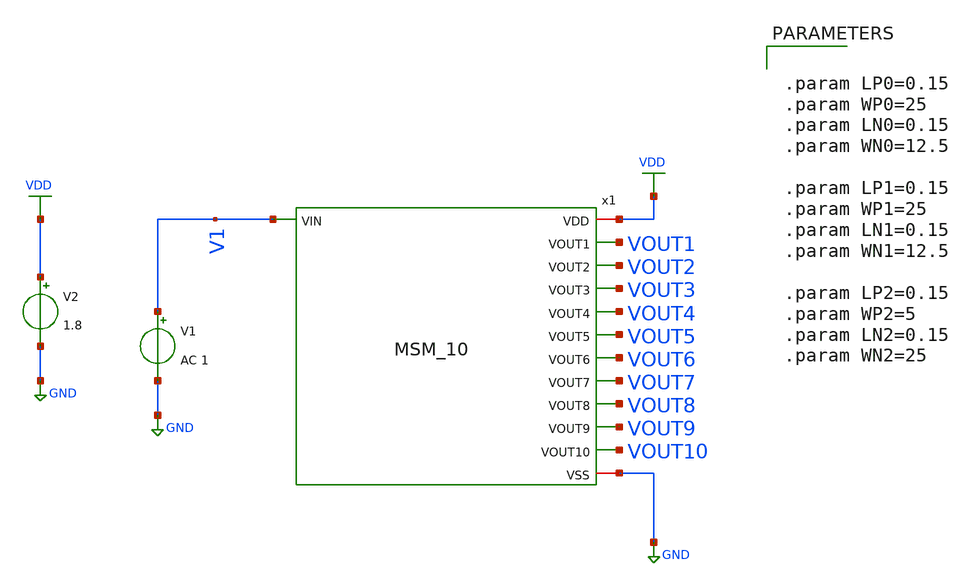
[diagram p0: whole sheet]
** sch_path: LIQAF circuit/10-Stage/DC Sweep.sch
**.subckt DC Sweep
V1 V1 GND AC 1
V2 VDD GND 1.8
x1 VDD VOUT1 VOUT2 V1 VOUT3 VOUT4 VOUT5 VOUT6 VOUT7 VOUT8 VOUT9 VOUT10 GND MSM_10
**** begin user architecture code
 ** manual skywater pdks install (with patches applied)
* .lib $::SKYWATER_MODELS/models/sky130.lib.spice tt

** opencircuitdesign pdks install
.lib $::SKYWATER_MODELS/sky130.lib.spice tt

.param mc_mm_switch=0
.param mc_pr_switch=0


.dc V1 0 1.8 0.01
.control
run
plot v(V1) v(VOUT1) v(VOUT2) v(VOUT3) v(VOUT4) v(VOUT5) v(VOUT6) v(VOUT7) v(VOUT8) v(VOUT9)
+ v(VOUT10)
.endc
.save all



.param LP0=0.15
.param WP0=25
.param LN0=0.15
.param WN0=12.5

.param LP1=0.15
.param WP1=25
.param LN1=0.15
.param WN1=12.5

.param LP2=0.15
.param WP2=5
.param LN2=0.15
.param WN2=25


**** end user architecture code
**.ends

* expanding   symbol:  /home/sudhar/Documents/VLSI/Analog-MSM-Array/LIQAF
*+ circuit/10-Stage/MSM_10.sym # of pins=13
** sym_path: LIQAF circuit/10-Stage/MSM_10.sym
** sch_path: LIQAF circuit/10-Stage/MSM_10.sch
.subckt MSM_10 VDD VOUT1 VOUT2 VIN VOUT3 VOUT4 VOUT5 VOUT6 VOUT7 VOUT8 VOUT9 VOUT10 VSS
*.ipin VIN
*.iopin VDD
*.iopin VSS
*.opin VOUT1
*.opin VOUT2
*.opin VOUT3
*.opin VOUT4
*.opin VOUT5
*.opin VOUT6
*.opin VOUT7
*.opin VOUT8
*.opin VOUT9
*.opin VOUT10
XM1 VOUT1 VIN VOUT2 VSS sky130_fd_pr__nfet_01v8 L=LN1 W=WN1 nf=1 ad='int((nf+1)/2) * W/nf * 0.29' as='int((nf+2)/2) * W/nf * 0.29'
+ pd='2*int((nf+1)/2) * (W/nf + 0.29)' ps='2*int((nf+2)/2) * (W/nf + 0.29)' nrd='0.29 / W' nrs='0.29 / W'
+ sa=0 sb=0 sd=0 mult=1 m=1
XM2 VOUT10 VIN VSS VSS sky130_fd_pr__nfet_01v8 L=LN0 W=WN0 nf=1 ad='int((nf+1)/2) * W/nf * 0.29' as='int((nf+2)/2) * W/nf * 0.29'
+ pd='2*int((nf+1)/2) * (W/nf + 0.29)' ps='2*int((nf+2)/2) * (W/nf + 0.29)' nrd='0.29 / W' nrs='0.29 / W'
+ sa=0 sb=0 sd=0 mult=1 m=1
XM3 VOUT2 VIN VOUT1 VDD sky130_fd_pr__pfet_01v8 L=LP1 W=WP1 nf=1 ad='int((nf+1)/2) * W/nf * 0.29' as='int((nf+2)/2) * W/nf * 0.29'
+ pd='2*int((nf+1)/2) * (W/nf + 0.29)' ps='2*int((nf+2)/2) * (W/nf + 0.29)' nrd='0.29 / W' nrs='0.29 / W'
+ sa=0 sb=0 sd=0 mult=1 m=1
XM4 VOUT1 VIN VDD VDD sky130_fd_pr__pfet_01v8 L=LP0 W=WP0 nf=1 ad='int((nf+1)/2) * W/nf * 0.29' as='int((nf+2)/2) * W/nf * 0.29'
+ pd='2*int((nf+1)/2) * (W/nf + 0.29)' ps='2*int((nf+2)/2) * (W/nf + 0.29)' nrd='0.29 / W' nrs='0.29 / W'
+ sa=0 sb=0 sd=0 mult=1 m=1
XM5 VOUT1 VDD net1 VSS sky130_fd_pr__nfet_01v8 L=LN2 W=WN2 nf=1 ad='int((nf+1)/2) * W/nf * 0.29' as='int((nf+2)/2) * W/nf * 0.29'
+ pd='2*int((nf+1)/2) * (W/nf + 0.29)' ps='2*int((nf+2)/2) * (W/nf + 0.29)' nrd='0.29 / W' nrs='0.29 / W'
+ sa=0 sb=0 sd=0 mult=1 m=1
XM6 VIN VOUT2 net1 VDD sky130_fd_pr__pfet_01v8 L=LP2 W=WP2 nf=1 ad='int((nf+1)/2) * W/nf * 0.29' as='int((nf+2)/2) * W/nf * 0.29'
+ pd='2*int((nf+1)/2) * (W/nf + 0.29)' ps='2*int((nf+2)/2) * (W/nf + 0.29)' nrd='0.29 / W' nrs='0.29 / W'
+ sa=0 sb=0 sd=0 mult=1 m=1
XM7 VOUT2 VOUT1 net2 VSS sky130_fd_pr__nfet_01v8 L=LN2 W=WN2 nf=1 ad='int((nf+1)/2) * W/nf * 0.29' as='int((nf+2)/2) * W/nf * 0.29'
+ pd='2*int((nf+1)/2) * (W/nf + 0.29)' ps='2*int((nf+2)/2) * (W/nf + 0.29)' nrd='0.29 / W' nrs='0.29 / W'
+ sa=0 sb=0 sd=0 mult=1 m=1
XM8 VIN VOUT3 net2 VDD sky130_fd_pr__pfet_01v8 L=LP2 W=WP2 nf=1 ad='int((nf+1)/2) * W/nf * 0.29' as='int((nf+2)/2) * W/nf * 0.29'
+ pd='2*int((nf+1)/2) * (W/nf + 0.29)' ps='2*int((nf+2)/2) * (W/nf + 0.29)' nrd='0.29 / W' nrs='0.29 / W'
+ sa=0 sb=0 sd=0 mult=1 m=1
XM9 VOUT2 VIN VOUT3 VSS sky130_fd_pr__nfet_01v8 L=LN1 W=WN1 nf=1 ad='int((nf+1)/2) * W/nf * 0.29' as='int((nf+2)/2) * W/nf * 0.29'
+ pd='2*int((nf+1)/2) * (W/nf + 0.29)' ps='2*int((nf+2)/2) * (W/nf + 0.29)' nrd='0.29 / W' nrs='0.29 / W'
+ sa=0 sb=0 sd=0 mult=1 m=1
XM10 VOUT3 VIN VOUT2 VDD sky130_fd_pr__pfet_01v8 L=LP1 W=WP1 nf=1 ad='int((nf+1)/2) * W/nf * 0.29' as='int((nf+2)/2) * W/nf * 0.29'
+ pd='2*int((nf+1)/2) * (W/nf + 0.29)' ps='2*int((nf+2)/2) * (W/nf + 0.29)' nrd='0.29 / W' nrs='0.29 / W'
+ sa=0 sb=0 sd=0 mult=1 m=1
XM11 VOUT3 VIN VOUT4 VSS sky130_fd_pr__nfet_01v8 L=LN1 W=WN1 nf=1 ad='int((nf+1)/2) * W/nf * 0.29' as='int((nf+2)/2) * W/nf * 0.29'
+ pd='2*int((nf+1)/2) * (W/nf + 0.29)' ps='2*int((nf+2)/2) * (W/nf + 0.29)' nrd='0.29 / W' nrs='0.29 / W'
+ sa=0 sb=0 sd=0 mult=1 m=1
XM12 VOUT4 VIN VOUT3 VDD sky130_fd_pr__pfet_01v8 L=LP1 W=WP1 nf=1 ad='int((nf+1)/2) * W/nf * 0.29' as='int((nf+2)/2) * W/nf * 0.29'
+ pd='2*int((nf+1)/2) * (W/nf + 0.29)' ps='2*int((nf+2)/2) * (W/nf + 0.29)' nrd='0.29 / W' nrs='0.29 / W'
+ sa=0 sb=0 sd=0 mult=1 m=1
XM13 VOUT4 VIN VOUT5 VSS sky130_fd_pr__nfet_01v8 L=LN1 W=WN1 nf=1 ad='int((nf+1)/2) * W/nf * 0.29' as='int((nf+2)/2) * W/nf * 0.29'
+ pd='2*int((nf+1)/2) * (W/nf + 0.29)' ps='2*int((nf+2)/2) * (W/nf + 0.29)' nrd='0.29 / W' nrs='0.29 / W'
+ sa=0 sb=0 sd=0 mult=1 m=1
XM14 VOUT5 VIN VOUT4 VDD sky130_fd_pr__pfet_01v8 L=LP1 W=WP1 nf=1 ad='int((nf+1)/2) * W/nf * 0.29' as='int((nf+2)/2) * W/nf * 0.29'
+ pd='2*int((nf+1)/2) * (W/nf + 0.29)' ps='2*int((nf+2)/2) * (W/nf + 0.29)' nrd='0.29 / W' nrs='0.29 / W'
+ sa=0 sb=0 sd=0 mult=1 m=1
XM15 VOUT5 VIN VOUT6 VSS sky130_fd_pr__nfet_01v8 L=LN1 W=WN1 nf=1 ad='int((nf+1)/2) * W/nf * 0.29' as='int((nf+2)/2) * W/nf * 0.29'
+ pd='2*int((nf+1)/2) * (W/nf + 0.29)' ps='2*int((nf+2)/2) * (W/nf + 0.29)' nrd='0.29 / W' nrs='0.29 / W'
+ sa=0 sb=0 sd=0 mult=1 m=1
XM16 VOUT6 VIN VOUT5 VDD sky130_fd_pr__pfet_01v8 L=LP1 W=WP1 nf=1 ad='int((nf+1)/2) * W/nf * 0.29' as='int((nf+2)/2) * W/nf * 0.29'
+ pd='2*int((nf+1)/2) * (W/nf + 0.29)' ps='2*int((nf+2)/2) * (W/nf + 0.29)' nrd='0.29 / W' nrs='0.29 / W'
+ sa=0 sb=0 sd=0 mult=1 m=1
XM17 VOUT6 VIN VOUT7 VSS sky130_fd_pr__nfet_01v8 L=LN1 W=WN1 nf=1 ad='int((nf+1)/2) * W/nf * 0.29' as='int((nf+2)/2) * W/nf * 0.29'
+ pd='2*int((nf+1)/2) * (W/nf + 0.29)' ps='2*int((nf+2)/2) * (W/nf + 0.29)' nrd='0.29 / W' nrs='0.29 / W'
+ sa=0 sb=0 sd=0 mult=1 m=1
XM18 VOUT7 VIN VOUT6 VDD sky130_fd_pr__pfet_01v8 L=LP1 W=WP1 nf=1 ad='int((nf+1)/2) * W/nf * 0.29' as='int((nf+2)/2) * W/nf * 0.29'
+ pd='2*int((nf+1)/2) * (W/nf + 0.29)' ps='2*int((nf+2)/2) * (W/nf + 0.29)' nrd='0.29 / W' nrs='0.29 / W'
+ sa=0 sb=0 sd=0 mult=1 m=1
XM19 VOUT7 VIN VOUT8 VSS sky130_fd_pr__nfet_01v8 L=LN1 W=WN1 nf=1 ad='int((nf+1)/2) * W/nf * 0.29' as='int((nf+2)/2) * W/nf * 0.29'
+ pd='2*int((nf+1)/2) * (W/nf + 0.29)' ps='2*int((nf+2)/2) * (W/nf + 0.29)' nrd='0.29 / W' nrs='0.29 / W'
+ sa=0 sb=0 sd=0 mult=1 m=1
XM20 VOUT8 VIN VOUT7 VDD sky130_fd_pr__pfet_01v8 L=LP1 W=WP1 nf=1 ad='int((nf+1)/2) * W/nf * 0.29' as='int((nf+2)/2) * W/nf * 0.29'
+ pd='2*int((nf+1)/2) * (W/nf + 0.29)' ps='2*int((nf+2)/2) * (W/nf + 0.29)' nrd='0.29 / W' nrs='0.29 / W'
+ sa=0 sb=0 sd=0 mult=1 m=1
XM21 VOUT8 VIN VOUT9 VSS sky130_fd_pr__nfet_01v8 L=LN1 W=WN1 nf=1 ad='int((nf+1)/2) * W/nf * 0.29' as='int((nf+2)/2) * W/nf * 0.29'
+ pd='2*int((nf+1)/2) * (W/nf + 0.29)' ps='2*int((nf+2)/2) * (W/nf + 0.29)' nrd='0.29 / W' nrs='0.29 / W'
+ sa=0 sb=0 sd=0 mult=1 m=1
XM22 VOUT9 VIN VOUT8 VDD sky130_fd_pr__pfet_01v8 L=LP1 W=WP1 nf=1 ad='int((nf+1)/2) * W/nf * 0.29' as='int((nf+2)/2) * W/nf * 0.29'
+ pd='2*int((nf+1)/2) * (W/nf + 0.29)' ps='2*int((nf+2)/2) * (W/nf + 0.29)' nrd='0.29 / W' nrs='0.29 / W'
+ sa=0 sb=0 sd=0 mult=1 m=1
XM23 VOUT9 VIN VOUT10 VSS sky130_fd_pr__nfet_01v8 L=LN1 W=WN1 nf=1 ad='int((nf+1)/2) * W/nf * 0.29' as='int((nf+2)/2) * W/nf * 0.29'
+ pd='2*int((nf+1)/2) * (W/nf + 0.29)' ps='2*int((nf+2)/2) * (W/nf + 0.29)' nrd='0.29 / W' nrs='0.29 / W'
+ sa=0 sb=0 sd=0 mult=1 m=1
XM24 VOUT10 VIN VOUT9 VDD sky130_fd_pr__pfet_01v8 L=LP1 W=WP1 nf=1 ad='int((nf+1)/2) * W/nf * 0.29' as='int((nf+2)/2) * W/nf * 0.29'
+ pd='2*int((nf+1)/2) * (W/nf + 0.29)' ps='2*int((nf+2)/2) * (W/nf + 0.29)' nrd='0.29 / W' nrs='0.29 / W'
+ sa=0 sb=0 sd=0 mult=1 m=1
XM25 VOUT3 VOUT2 net3 VSS sky130_fd_pr__nfet_01v8 L=LN2 W=WN2 nf=1 ad='int((nf+1)/2) * W/nf * 0.29' as='int((nf+2)/2) * W/nf * 0.29'
+ pd='2*int((nf+1)/2) * (W/nf + 0.29)' ps='2*int((nf+2)/2) * (W/nf + 0.29)' nrd='0.29 / W' nrs='0.29 / W'
+ sa=0 sb=0 sd=0 mult=1 m=1
XM26 VIN VOUT4 net3 VDD sky130_fd_pr__pfet_01v8 L=LP2 W=WP2 nf=1 ad='int((nf+1)/2) * W/nf * 0.29' as='int((nf+2)/2) * W/nf * 0.29'
+ pd='2*int((nf+1)/2) * (W/nf + 0.29)' ps='2*int((nf+2)/2) * (W/nf + 0.29)' nrd='0.29 / W' nrs='0.29 / W'
+ sa=0 sb=0 sd=0 mult=1 m=1
XM27 VOUT4 VOUT3 net4 VSS sky130_fd_pr__nfet_01v8 L=LN2 W=WN2 nf=1 ad='int((nf+1)/2) * W/nf * 0.29' as='int((nf+2)/2) * W/nf * 0.29'
+ pd='2*int((nf+1)/2) * (W/nf + 0.29)' ps='2*int((nf+2)/2) * (W/nf + 0.29)' nrd='0.29 / W' nrs='0.29 / W'
+ sa=0 sb=0 sd=0 mult=1 m=1
XM28 VIN VOUT5 net4 VDD sky130_fd_pr__pfet_01v8 L=LP2 W=WP2 nf=1 ad='int((nf+1)/2) * W/nf * 0.29' as='int((nf+2)/2) * W/nf * 0.29'
+ pd='2*int((nf+1)/2) * (W/nf + 0.29)' ps='2*int((nf+2)/2) * (W/nf + 0.29)' nrd='0.29 / W' nrs='0.29 / W'
+ sa=0 sb=0 sd=0 mult=1 m=1
XM29 VOUT5 VOUT4 net5 VSS sky130_fd_pr__nfet_01v8 L=LN2 W=WN2 nf=1 ad='int((nf+1)/2) * W/nf * 0.29' as='int((nf+2)/2) * W/nf * 0.29'
+ pd='2*int((nf+1)/2) * (W/nf + 0.29)' ps='2*int((nf+2)/2) * (W/nf + 0.29)' nrd='0.29 / W' nrs='0.29 / W'
+ sa=0 sb=0 sd=0 mult=1 m=1
XM30 VIN VOUT6 net5 VDD sky130_fd_pr__pfet_01v8 L=LP2 W=WP2 nf=1 ad='int((nf+1)/2) * W/nf * 0.29' as='int((nf+2)/2) * W/nf * 0.29'
+ pd='2*int((nf+1)/2) * (W/nf + 0.29)' ps='2*int((nf+2)/2) * (W/nf + 0.29)' nrd='0.29 / W' nrs='0.29 / W'
+ sa=0 sb=0 sd=0 mult=1 m=1
XM31 VOUT6 VOUT5 net6 VSS sky130_fd_pr__nfet_01v8 L=LN2 W=WN2 nf=1 ad='int((nf+1)/2) * W/nf * 0.29' as='int((nf+2)/2) * W/nf * 0.29'
+ pd='2*int((nf+1)/2) * (W/nf + 0.29)' ps='2*int((nf+2)/2) * (W/nf + 0.29)' nrd='0.29 / W' nrs='0.29 / W'
+ sa=0 sb=0 sd=0 mult=1 m=1
XM32 VIN VOUT7 net6 VDD sky130_fd_pr__pfet_01v8 L=LP2 W=WP2 nf=1 ad='int((nf+1)/2) * W/nf * 0.29' as='int((nf+2)/2) * W/nf * 0.29'
+ pd='2*int((nf+1)/2) * (W/nf + 0.29)' ps='2*int((nf+2)/2) * (W/nf + 0.29)' nrd='0.29 / W' nrs='0.29 / W'
+ sa=0 sb=0 sd=0 mult=1 m=1
XM33 VOUT7 VOUT6 net7 VSS sky130_fd_pr__nfet_01v8 L=LN2 W=WN2 nf=1 ad='int((nf+1)/2) * W/nf * 0.29' as='int((nf+2)/2) * W/nf * 0.29'
+ pd='2*int((nf+1)/2) * (W/nf + 0.29)' ps='2*int((nf+2)/2) * (W/nf + 0.29)' nrd='0.29 / W' nrs='0.29 / W'
+ sa=0 sb=0 sd=0 mult=1 m=1
XM34 VIN VOUT8 net7 VDD sky130_fd_pr__pfet_01v8 L=LP2 W=WP2 nf=1 ad='int((nf+1)/2) * W/nf * 0.29' as='int((nf+2)/2) * W/nf * 0.29'
+ pd='2*int((nf+1)/2) * (W/nf + 0.29)' ps='2*int((nf+2)/2) * (W/nf + 0.29)' nrd='0.29 / W' nrs='0.29 / W'
+ sa=0 sb=0 sd=0 mult=1 m=1
XM35 VOUT8 VOUT7 net8 VSS sky130_fd_pr__nfet_01v8 L=LN2 W=WN2 nf=1 ad='int((nf+1)/2) * W/nf * 0.29' as='int((nf+2)/2) * W/nf * 0.29'
+ pd='2*int((nf+1)/2) * (W/nf + 0.29)' ps='2*int((nf+2)/2) * (W/nf + 0.29)' nrd='0.29 / W' nrs='0.29 / W'
+ sa=0 sb=0 sd=0 mult=1 m=1
XM36 VIN VOUT9 net8 VDD sky130_fd_pr__pfet_01v8 L=LP2 W=WP2 nf=1 ad='int((nf+1)/2) * W/nf * 0.29' as='int((nf+2)/2) * W/nf * 0.29'
+ pd='2*int((nf+1)/2) * (W/nf + 0.29)' ps='2*int((nf+2)/2) * (W/nf + 0.29)' nrd='0.29 / W' nrs='0.29 / W'
+ sa=0 sb=0 sd=0 mult=1 m=1
XM37 VOUT9 VOUT8 net9 VSS sky130_fd_pr__nfet_01v8 L=LN2 W=WN2 nf=1 ad='int((nf+1)/2) * W/nf * 0.29' as='int((nf+2)/2) * W/nf * 0.29'
+ pd='2*int((nf+1)/2) * (W/nf + 0.29)' ps='2*int((nf+2)/2) * (W/nf + 0.29)' nrd='0.29 / W' nrs='0.29 / W'
+ sa=0 sb=0 sd=0 mult=1 m=1
XM38 VIN VOUT10 net9 VDD sky130_fd_pr__pfet_01v8 L=LP2 W=WP2 nf=1 ad='int((nf+1)/2) * W/nf * 0.29' as='int((nf+2)/2) * W/nf * 0.29'
+ pd='2*int((nf+1)/2) * (W/nf + 0.29)' ps='2*int((nf+2)/2) * (W/nf + 0.29)' nrd='0.29 / W' nrs='0.29 / W'
+ sa=0 sb=0 sd=0 mult=1 m=1
XM39 VOUT10 VOUT9 net10 VSS sky130_fd_pr__nfet_01v8 L=LN2 W=WN2 nf=1 ad='int((nf+1)/2) * W/nf * 0.29'
+ as='int((nf+2)/2) * W/nf * 0.29' pd='2*int((nf+1)/2) * (W/nf + 0.29)' ps='2*int((nf+2)/2) * (W/nf + 0.29)'
+ nrd='0.29 / W' nrs='0.29 / W' sa=0 sb=0 sd=0 mult=1 m=1
XM40 VIN VSS net10 VDD sky130_fd_pr__pfet_01v8 L=LP2 W=WP2 nf=1 ad='int((nf+1)/2) * W/nf * 0.29' as='int((nf+2)/2) * W/nf * 0.29'
+ pd='2*int((nf+1)/2) * (W/nf + 0.29)' ps='2*int((nf+2)/2) * (W/nf + 0.29)' nrd='0.29 / W' nrs='0.29 / W'
+ sa=0 sb=0 sd=0 mult=1 m=1
.ends

.GLOBAL GND
.GLOBAL VDD
.end
